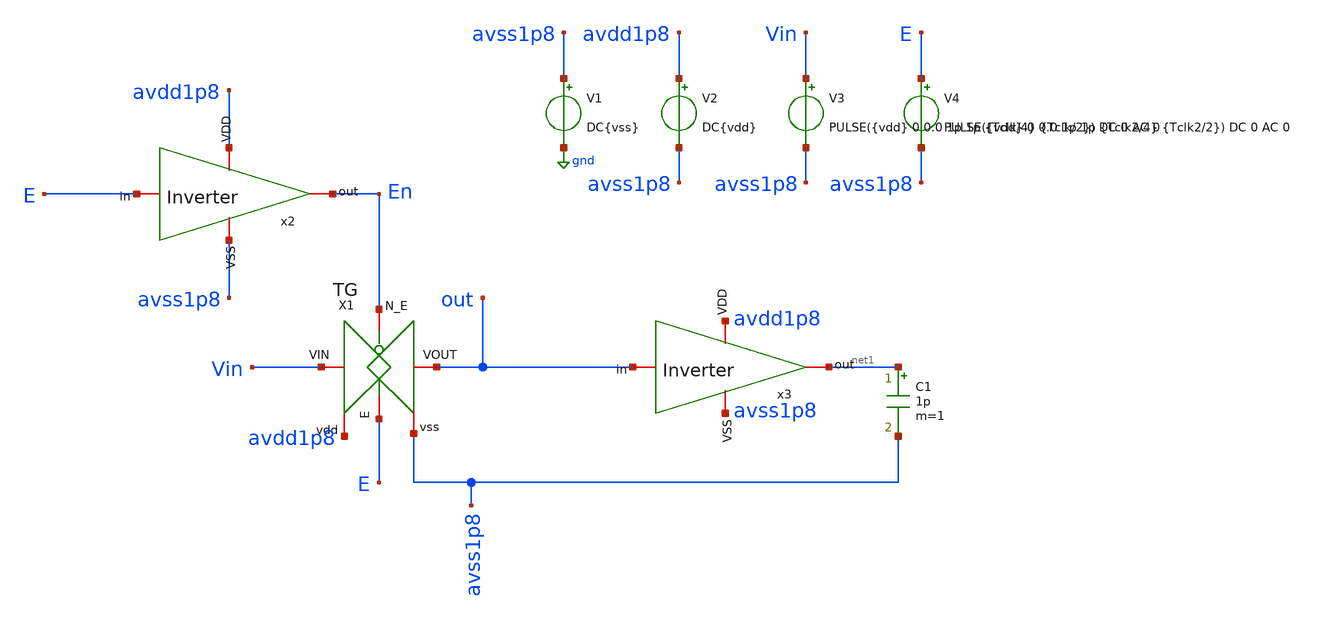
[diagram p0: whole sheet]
** sch_path: verification/testbenches/tb_tg.sch
**.subckt tb_tg
x1 E net2 out Vin avdd1p8 En tg
V1 avss1p8 gnd DC{vss}
V2 avdd1p8 avss1p8 DC{vdd}
V3 Vin avss1p8 PULSE({vdd} 0 0.0 1p 1p {Tclk/4} {Tclk/2}) DC 0 AC 0
V4 E avss1p8 PULSE({vdd} 0 0.0 1p 1p {Tclk2/4} {Tclk2/2}) DC 0 AC 0
x2 avdd1p8 En E avss1p8 inverter
x3 avdd1p8 net1 out avss1p8 inverter
C1 net1 avss1p8 1p m=1
**** begin user architecture code


* Circuit Parameters
.param vdd = 1.2
.param vss = 0.0
.param Tclk = 10n
.param Tclk2 = 100n
.options TEMP = 27.0
* Include Models - IHP SG13G2
.lib cornerMOSlv.lib mos_tt
* OP Parameters & Singals to save
.save all
*Simulations
.control
tran 0.01u 100n
setplot tran1
plot v(E) v(En)+1.5 v(out)+3 v(vin)+4.5
reset
set filetype = ascii
write dcsweep.raw
.endc
.end


**** end user architecture code
**.ends
.GLOBAL gnd
.end
